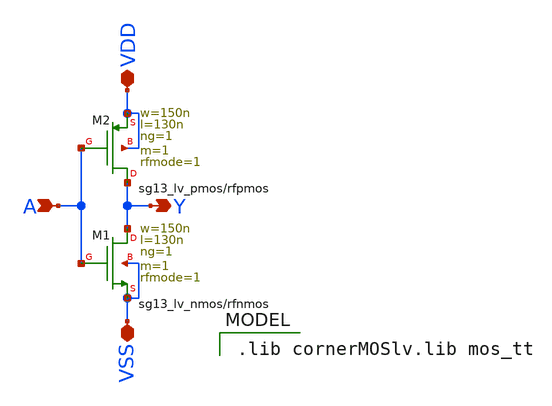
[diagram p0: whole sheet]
** sch_path: xschem/inverter.sch
**.subckt inverter A Y VDD VSS
*.ipin A
*.opin Y
*.iopin VDD
*.iopin VSS
XM1 Y A VSS VSS sg13_lv_nmos w=150n l=130n ng=1 m=1 rfmode=1 mm_ok=1
XM2 Y A VDD VDD sg13_lv_pmos w=150n l=130n ng=1 m=1 rfmode=1 mm_ok=1
**** begin user architecture code

.lib cornerMOSlv.lib mos_tt

**** end user architecture code
**.ends
.end
